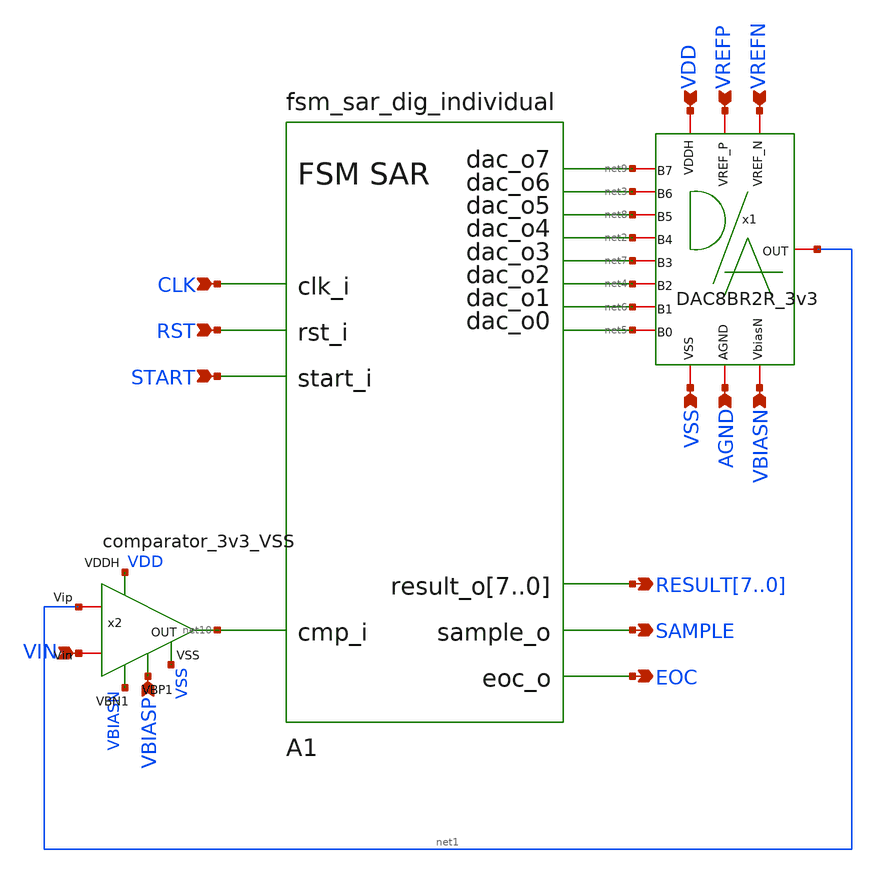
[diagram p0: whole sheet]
** sch_path: Schematics/ADC/ADC.sch
**.subckt ADC CLK RST START VDD VREFN VREFP VBIASN AGND
*+ RESULT7,RESULT6,RESULT5,RESULT4,RESULT3,RESULT2,RESULT1,RESULT0 SAMPLE EOC VIN VBIASP VSS
*.ipin CLK
*.ipin RST
*.ipin START
*.ipin VDD
*.ipin VREFN
*.ipin VREFP
*.ipin VBIASN
*.ipin AGND
*.opin RESULT7,RESULT6,RESULT5,RESULT4,RESULT3,RESULT2,RESULT1,RESULT0
*.opin SAMPLE
*.opin EOC
*.ipin VIN
*.ipin VBIASP
*.ipin VSS
x1 VSS VBIASN AGND net1 VDD VREFN VREFP net2 net3 net4 net5 net6 net7 net8 net9 DAC8BR2R_3v3
A1 [ CLK RST START net10 ] [ RESULT7 RESULT6 RESULT5 RESULT4 RESULT3 RESULT2 RESULT1 RESULT0 net9
+ net3 net8 net2 net7 net4 net6 net5 SAMPLE EOC ] fsm_sar_model
x2 VDD net1 VIN VBIASN VSS VBIASP net10 comparator_3v3_VSS
**.ends
**** begin user architecture code
.model fsm_sar_model d_cosim simulation="ivlng" sim_args=["/foss/designs/fsm_sar_cosim/fsm_sar"]
+ delay=0
**** end user architecture code
.end
